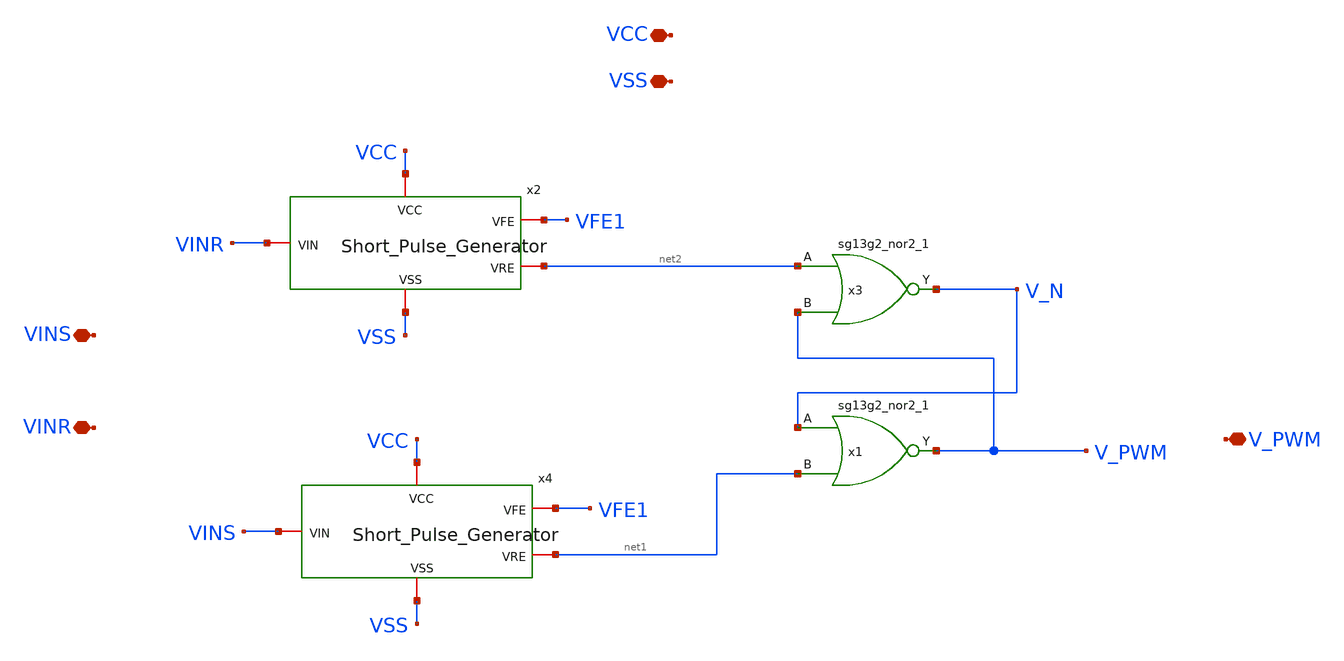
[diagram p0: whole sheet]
** sch_path: ChipUSM_AnalogTrack24/PD/PhaseDetector.sch
**.subckt PhaseDetector V_PWM VCC VSS VINS VINR
*.iopin V_PWM
*.iopin VCC
*.iopin VSS
*.iopin VINS
*.iopin VINR
x3 V_N net2 V_PWM VCC VSS sg13g2_nor2_1
x1 V_PWM V_N net1 VCC VSS sg13g2_nor2_1
x2 VCC VSS VFE1 VINR net2 Short_Pulse_Generator
x4 VCC VSS VFE1 VINS net1 Short_Pulse_Generator
**.ends
.end
